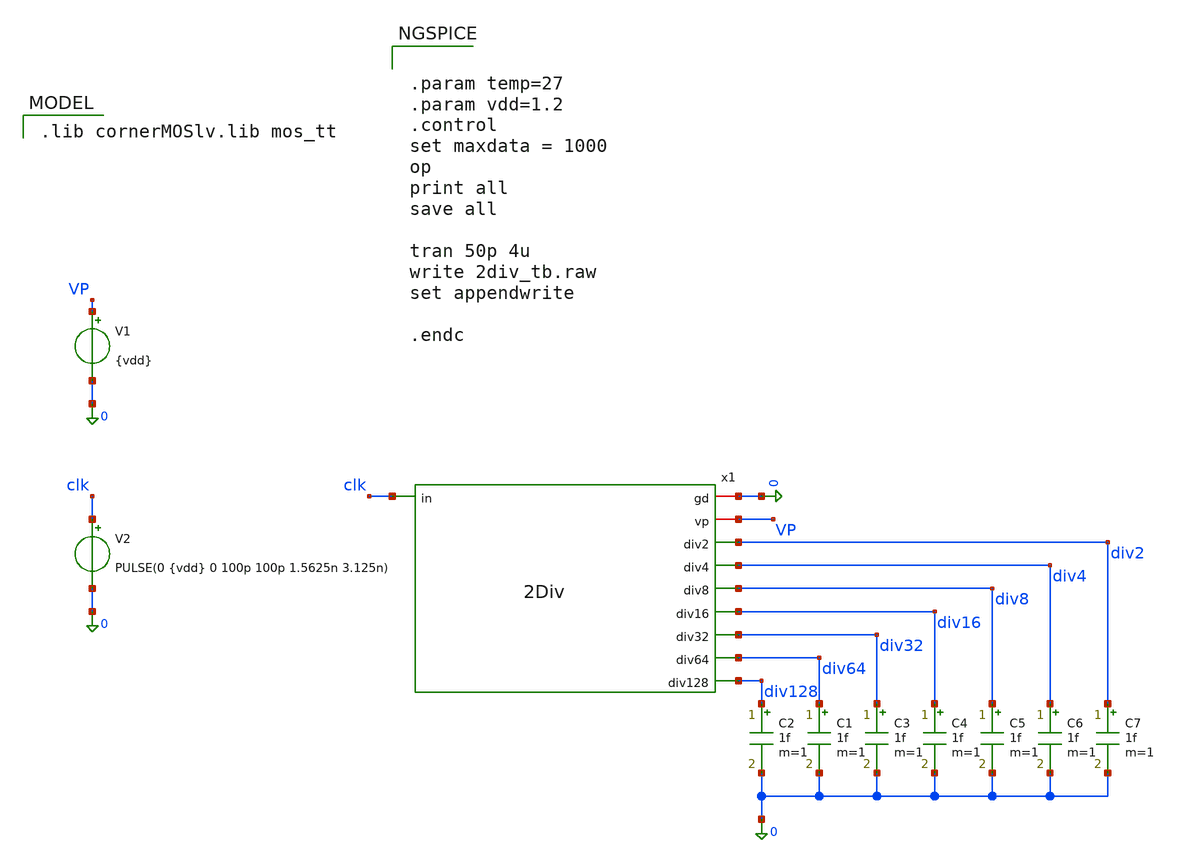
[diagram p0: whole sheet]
** sch_path: PLL0663-main/testbenches/tran/xschem/divider/2Div_tb.sch
**.subckt 2Div_tb
V1 VP 0 {vdd}
V2 clk 0 PULSE(0 {vdd} 0 100p 100p 1.5625n 3.125n)
C2 div128 0 1f m=1
C1 div64 0 1f m=1
C3 div32 0 1f m=1
C4 div16 0 1f m=1
C5 div8 0 1f m=1
C6 div4 0 1f m=1
C7 div2 0 1f m=1
x1 0 VP clk div2 div4 div8 div16 div32 div64 div128 2Div
**** begin user architecture code
 .lib cornerMOSlv.lib mos_tt



.param temp=27
.param vdd=1.2
.control
set maxdata = 1000
op
print all
save all

tran 50p 4u
write 2div_tb.raw
set appendwrite

.endc


**** end user architecture code
**.ends
.end
